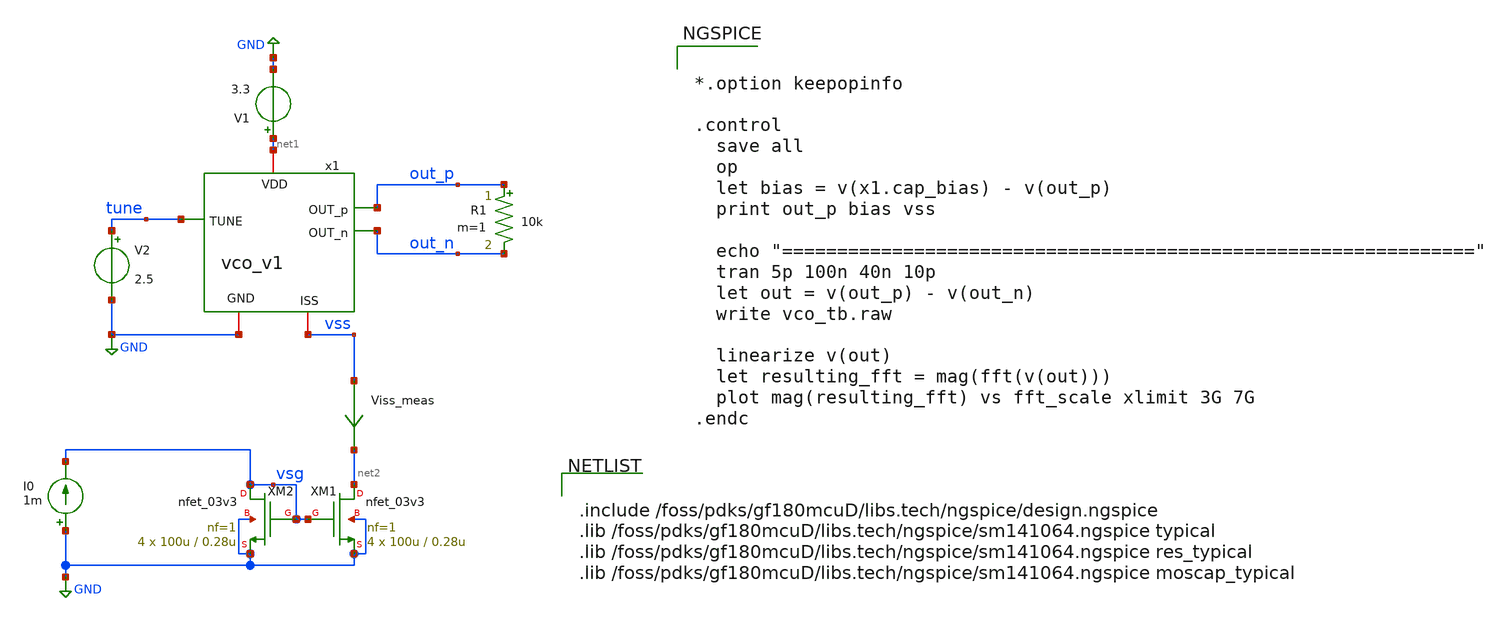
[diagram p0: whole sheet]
** sch_path: team_src/xschem/vco_tb.sch
**.subckt vco_tb
R1 out_p out_n 10k m=1
V1 net1 GND 3.3
.save i(v1)
x1 net1 out_p out_n GND tune vss vco_v1
V2 tune GND 2.5
.save i(v2)
XM2 vsg vsg GND GND nfet_03v3 L=0.28u W=100u nf=1 ad='int((nf+1)/2) * W/nf * 0.18u' as='int((nf+2)/2) * W/nf * 0.18u'
+ pd='2*int((nf+1)/2) * (W/nf + 0.18u)' ps='2*int((nf+2)/2) * (W/nf + 0.18u)' nrd='0.18u / W' nrs='0.18u / W'
+ sa=0 sb=0 sd=0 m=4
XM1 net2 vsg GND GND nfet_03v3 L=0.28u W=100u nf=1 ad='int((nf+1)/2) * W/nf * 0.18u' as='int((nf+2)/2) * W/nf * 0.18u'
+ pd='2*int((nf+1)/2) * (W/nf + 0.18u)' ps='2*int((nf+2)/2) * (W/nf + 0.18u)' nrd='0.18u / W' nrs='0.18u / W'
+ sa=0 sb=0 sd=0 m=4
Viss_meas vss net2 0
.save i(viss_meas)
I0 GND vsg 1m
**** begin user architecture code


*.option keepopinfo

.control
  save all
  op
  let bias = v(x1.cap_bias) - v(out_p)
  print out_p bias vss

  echo "==============================================================="
  tran 5p 100n 40n 10p
  let out = v(out_p) - v(out_n)
  write vco_tb.raw

  linearize v(out)
  let resulting_fft = mag(fft(v(out)))
  plot mag(resulting_fft) vs fft_scale xlimit 3G 7G
.endc




.include /foss/pdks/gf180mcuD/libs.tech/ngspice/design.ngspice
.lib /foss/pdks/gf180mcuD/libs.tech/ngspice/sm141064.ngspice typical
.lib /foss/pdks/gf180mcuD/libs.tech/ngspice/sm141064.ngspice res_typical
.lib /foss/pdks/gf180mcuD/libs.tech/ngspice/sm141064.ngspice moscap_typical


**** end user architecture code
**.ends

* expanding   symbol:  vco_v1.sym # of pins=6
** sym_path: team_src/xschem/vco_v1.sym
** sch_path: team_src/xschem/vco_v1.sch
.subckt vco_v1 VDD OUT_p OUT_n GND TUNE ISS
*.iopin VDD
*.iopin ISS
*.iopin GND
*.ipin TUNE
*.opin OUT_p
*.opin OUT_n
XM1 OUT_p OUT_n ISS ISS nfet_03v3 L=0.28u W=40u nf=1 ad='int((nf+1)/2) * W/nf * 0.18u' as='int((nf+2)/2) * W/nf * 0.18u'
+ pd='2*int((nf+1)/2) * (W/nf + 0.18u)' ps='2*int((nf+2)/2) * (W/nf + 0.18u)' nrd='0.18u / W' nrs='0.18u / W'
+ sa=0 sb=0 sd=0 m=1
XM2 OUT_p OUT_n VDD VDD pfet_03v3 L=0.28u W=70u nf=1 ad='int((nf+1)/2) * W/nf * 0.18u' as='int((nf+2)/2) * W/nf * 0.18u'
+ pd='2*int((nf+1)/2) * (W/nf + 0.18u)' ps='2*int((nf+2)/2) * (W/nf + 0.18u)' nrd='0.18u / W' nrs='0.18u / W'
+ sa=0 sb=0 sd=0 m=1
X1 OUT_n OUT_p GND vco_inductor_v2
XM3 OUT_n OUT_p VDD VDD pfet_03v3 L=0.28u W=70u nf=1 ad='int((nf+1)/2) * W/nf * 0.18u' as='int((nf+2)/2) * W/nf * 0.18u'
+ pd='2*int((nf+1)/2) * (W/nf + 0.18u)' ps='2*int((nf+2)/2) * (W/nf + 0.18u)' nrd='0.18u / W' nrs='0.18u / W'
+ sa=0 sb=0 sd=0 m=1
XM4 OUT_n OUT_p ISS ISS nfet_03v3 L=0.28u W=40u nf=1 ad='int((nf+1)/2) * W/nf * 0.18u' as='int((nf+2)/2) * W/nf * 0.18u'
+ pd='2*int((nf+1)/2) * (W/nf + 0.18u)' ps='2*int((nf+2)/2) * (W/nf + 0.18u)' nrd='0.18u / W' nrs='0.18u / W'
+ sa=0 sb=0 sd=0 m=1
XC1 cap_bias OUT_n cap_nmos_03v3_b c_width=5u c_length=5u m=21
XC4 cap_bias OUT_p cap_nmos_03v3_b c_width=5u c_length=5u m=21
XR2 TUNE cap_bias GND ppolyf_u_3k r_width=1u r_length=5u m=1
.ends


* expanding   symbol:  vco_inductor_v2.sym # of pins=3
** sym_path: team_src/xschem/vco_inductor_v2.sym
.include $UPRJ_ROOT/team_src/xschem/vco_inductor_v2.subckt
.GLOBAL GND
.end
